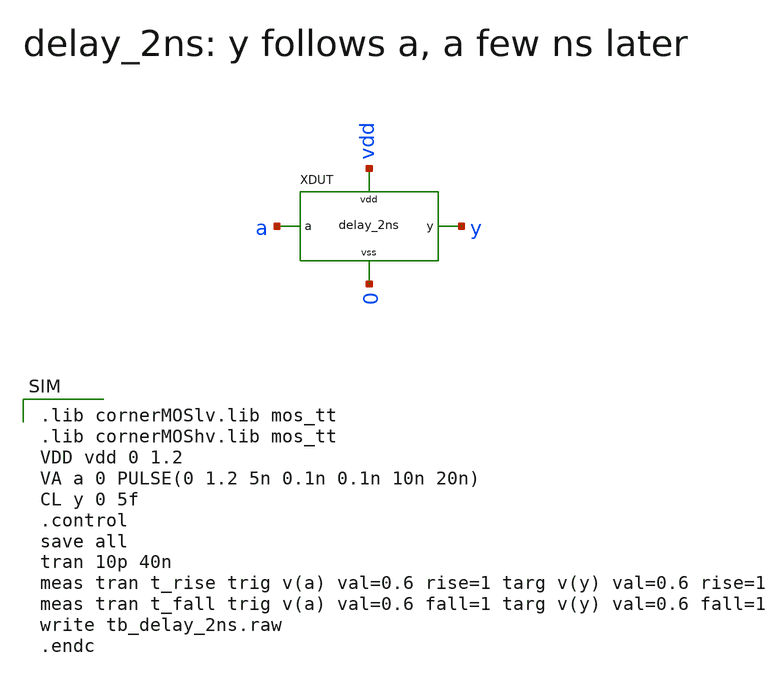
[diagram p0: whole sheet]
** sch_path: verification/tb_delay_2ns.sch
**.subckt tb_delay_2ns
XDUT a y vdd 0 delay_2ns
**** begin user architecture code

.lib cornerMOSlv.lib mos_tt
.lib cornerMOShv.lib mos_tt
VDD vdd 0 1.2
VA a 0 PULSE(0 1.2 5n 0.1n 0.1n 10n 20n)
CL y 0 5f
.control
save all
tran 10p 40n
meas tran t_rise trig v(a) val=0.6 rise=1 targ v(y) val=0.6 rise=1
meas tran t_fall trig v(a) val=0.6 fall=1 targ v(y) val=0.6 fall=1
write tb_delay_2ns.raw
.endc

**** end user architecture code
**.ends
.end
